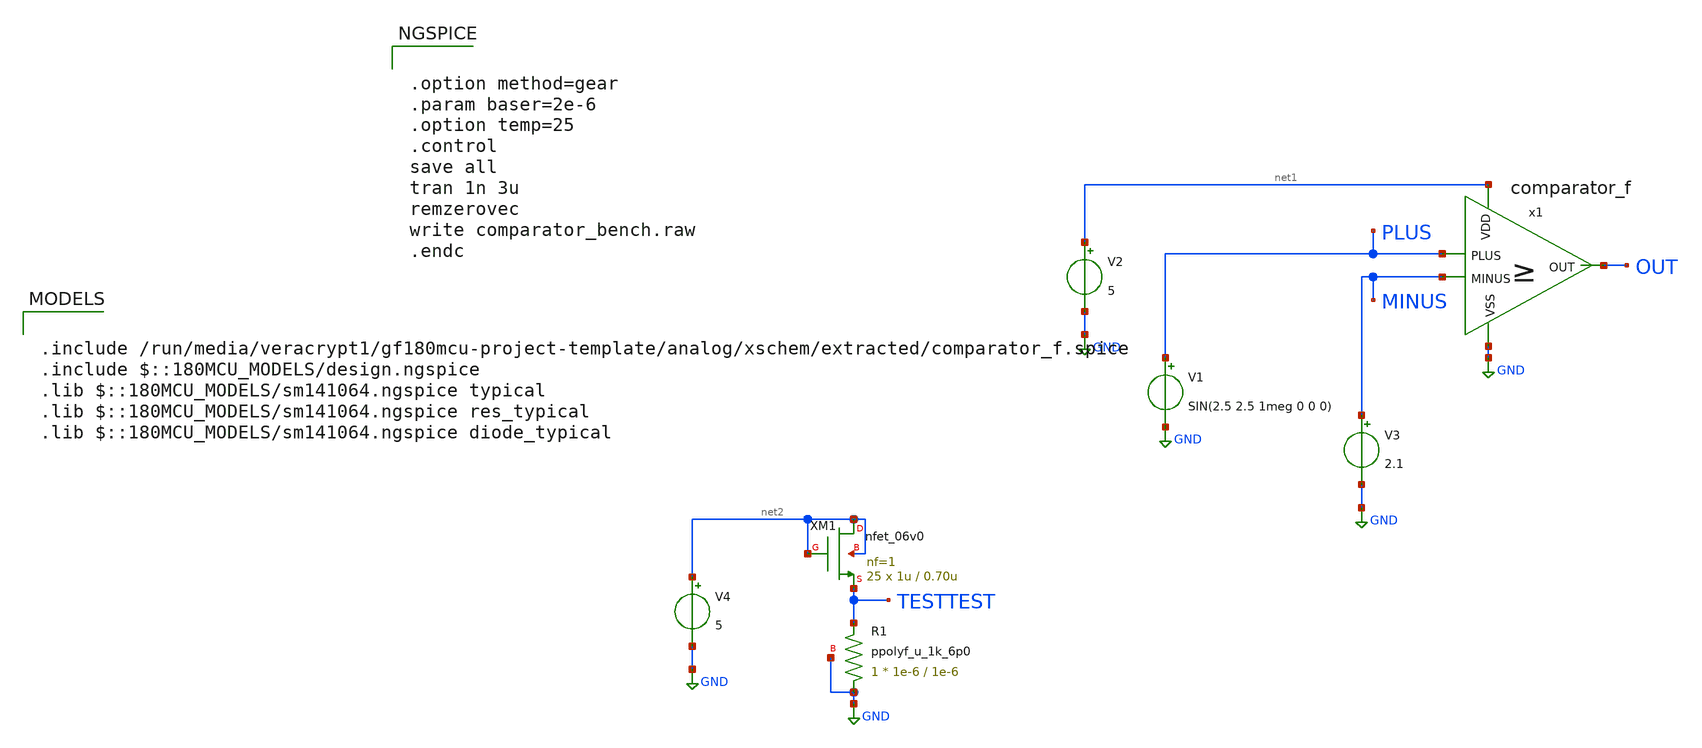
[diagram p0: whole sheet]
** sch_path: analog/xschem/comparator_bench.sch
**.subckt comparator_bench
V2 net1 GND 5
V1 PLUS GND SIN(2.5 2.5 1meg 0 0 0)
V3 MINUS GND 2.1
XR1 GND TESTTEST GND ppolyf_u_1k_6p0 r_width=1e-6 r_length=1e-6 m=1
V4 net2 GND 5
XM1 net2 net2 TESTTEST net2 nfet_06v0 L=0.70u W=1u nf=1 ad='int((nf+1)/2) * W/nf * 0.18u' as='int((nf+2)/2) * W/nf * 0.18u'
+ pd='2*int((nf+1)/2) * (W/nf + 0.18u)' ps='2*int((nf+2)/2) * (W/nf + 0.18u)' nrd='0.18u / W' nrs='0.18u / W'
+ sa=0 sb=0 sd=0 m=25
x1 net1 GND MINUS PLUS OUT comparator_f
**** begin user architecture code


.option method=gear
.param baser=2e-6
.option temp=25
.control
save all
tran 1n 3u
remzerovec
write comparator_bench.raw
.endc



.include /run/media/veracrypt1/gf180mcu-project-template/analog/xschem/extracted/comparator_f.spice
.include $::180MCU_MODELS/design.ngspice
.lib $::180MCU_MODELS/sm141064.ngspice typical
.lib $::180MCU_MODELS/sm141064.ngspice res_typical
.lib $::180MCU_MODELS/sm141064.ngspice diode_typical

**** end user architecture code
**.ends
.GLOBAL GND
.end
